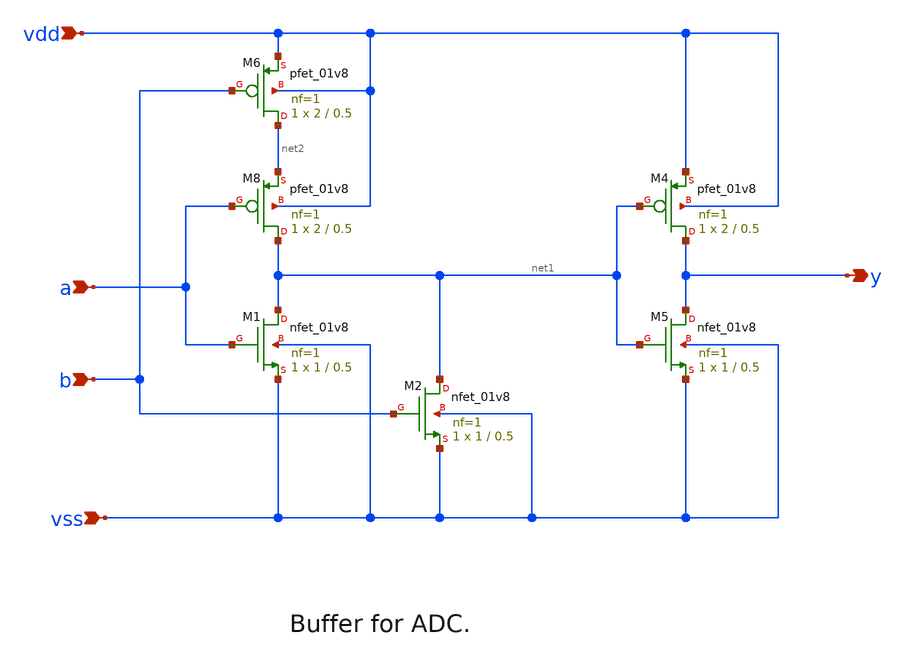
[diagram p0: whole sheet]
** sch_path: xschem/or.sch
**.subckt or vdd vss a b y
*.ipin vdd
*.ipin vss
*.ipin a
*.ipin b
*.opin y
XM2 net1 b vss vss sky130_fd_pr__nfet_01v8 L=0.5 W=1 nf=1 ad='int((nf+1)/2) * W/nf * 0.29' as='int((nf+2)/2) * W/nf * 0.29'
+ pd='2*int((nf+1)/2) * (W/nf + 0.29)' ps='2*int((nf+2)/2) * (W/nf + 0.29)' nrd='0.29 / W' nrs='0.29 / W'
+ sa=0 sb=0 sd=0 mult=1 m=1
XM8 net1 a net2 vdd sky130_fd_pr__pfet_01v8 L=0.5 W=2 nf=1 ad='int((nf+1)/2) * W/nf * 0.29' as='int((nf+2)/2) * W/nf * 0.29'
+ pd='2*int((nf+1)/2) * (W/nf + 0.29)' ps='2*int((nf+2)/2) * (W/nf + 0.29)' nrd='0.29 / W' nrs='0.29 / W'
+ sa=0 sb=0 sd=0 mult=1 m=1
XM1 net1 a vss vss sky130_fd_pr__nfet_01v8 L=0.5 W=1 nf=1 ad='int((nf+1)/2) * W/nf * 0.29' as='int((nf+2)/2) * W/nf * 0.29'
+ pd='2*int((nf+1)/2) * (W/nf + 0.29)' ps='2*int((nf+2)/2) * (W/nf + 0.29)' nrd='0.29 / W' nrs='0.29 / W'
+ sa=0 sb=0 sd=0 mult=1 m=1
XM4 y net1 vdd vdd sky130_fd_pr__pfet_01v8 L=0.5 W=2 nf=1 ad='int((nf+1)/2) * W/nf * 0.29' as='int((nf+2)/2) * W/nf * 0.29'
+ pd='2*int((nf+1)/2) * (W/nf + 0.29)' ps='2*int((nf+2)/2) * (W/nf + 0.29)' nrd='0.29 / W' nrs='0.29 / W'
+ sa=0 sb=0 sd=0 mult=1 m=1
XM5 y net1 vss vss sky130_fd_pr__nfet_01v8 L=0.5 W=1 nf=1 ad='int((nf+1)/2) * W/nf * 0.29' as='int((nf+2)/2) * W/nf * 0.29'
+ pd='2*int((nf+1)/2) * (W/nf + 0.29)' ps='2*int((nf+2)/2) * (W/nf + 0.29)' nrd='0.29 / W' nrs='0.29 / W'
+ sa=0 sb=0 sd=0 mult=1 m=1
XM6 net2 b vdd vdd sky130_fd_pr__pfet_01v8 L=0.5 W=2 nf=1 ad='int((nf+1)/2) * W/nf * 0.29' as='int((nf+2)/2) * W/nf * 0.29'
+ pd='2*int((nf+1)/2) * (W/nf + 0.29)' ps='2*int((nf+2)/2) * (W/nf + 0.29)' nrd='0.29 / W' nrs='0.29 / W'
+ sa=0 sb=0 sd=0 mult=1 m=1
**.ends
.end
